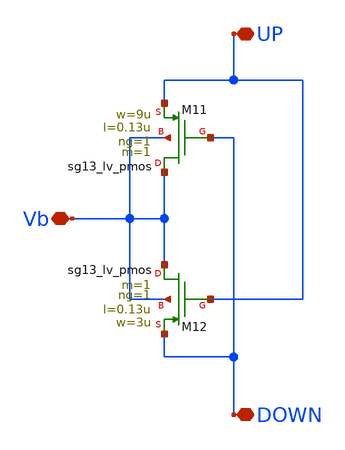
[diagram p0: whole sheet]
** sch_path: Layouts/Body_bias/untitled-13.sch
**.subckt untitled-13 UP DOWN Vb
*.iopin UP
*.iopin DOWN
*.iopin Vb
XM11 Vb DOWN UP Vb sg13_lv_pmos w=9u l=0.13u ng=1 m=1 mm_ok=1
XM12 Vb UP DOWN Vb sg13_lv_pmos w=3u l=0.13u ng=1 m=1 mm_ok=1
**.ends
.end
